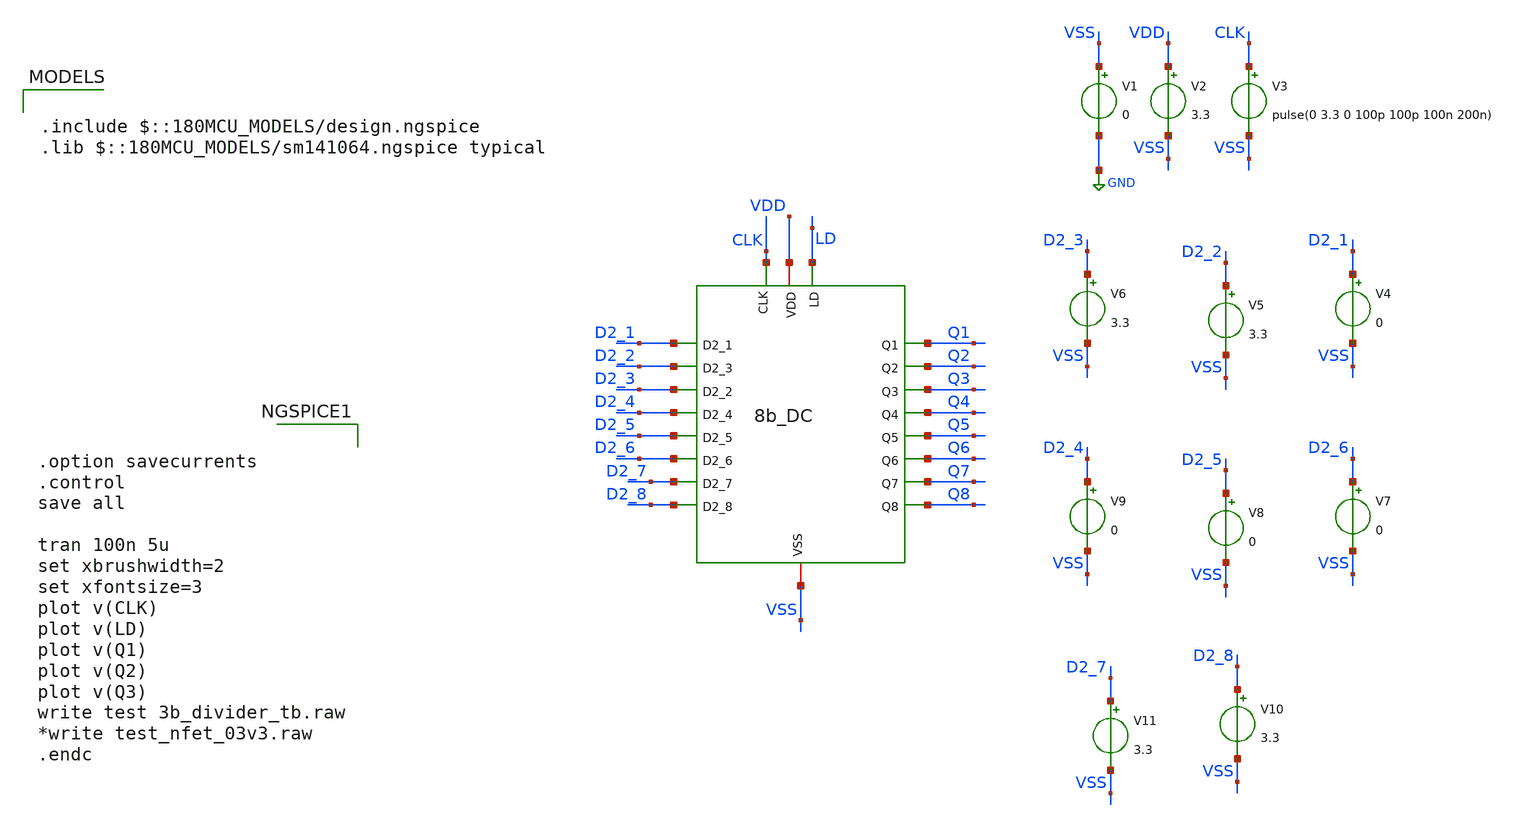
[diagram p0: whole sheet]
** sch_path: Clock_Generator_PAKISTAN_06/Xschem/8b_DC_tb.sch
**.subckt 8b_DC_tb
x1 LD VDD Q2 Q3 Q1 Q7 D2_2 Q6 D2_3 Q5 D2_1 Q8 CLK Q4 D2_8 D2_7 D2_6 D2_4 D2_5 VSS 8b_DC
V1 VSS GND 0
V2 VDD VSS 3.3
V3 CLK VSS pulse(0 3.3 0 100p 100p 100n 200n)
V4 D2_1 VSS 0
V5 D2_2 VSS 3.3
V6 D2_3 VSS 3.3
V7 D2_6 VSS 0
V8 D2_5 VSS 0
V9 D2_4 VSS 0
V10 D2_8 VSS 3.3
V11 D2_7 VSS 3.3
**** begin user architecture code

.include $::180MCU_MODELS/design.ngspice
.lib $::180MCU_MODELS/sm141064.ngspice typical



.option savecurrents
.control
save all

tran 100n 5u
set xbrushwidth=2
set xfontsize=3
plot v(CLK)
plot v(LD)
plot v(Q1)
plot v(Q2)
plot v(Q3)
write test 3b_divider_tb.raw
*write test_nfet_03v3.raw
.endc


**** end user architecture code
**.ends
.GLOBAL GND
.end
